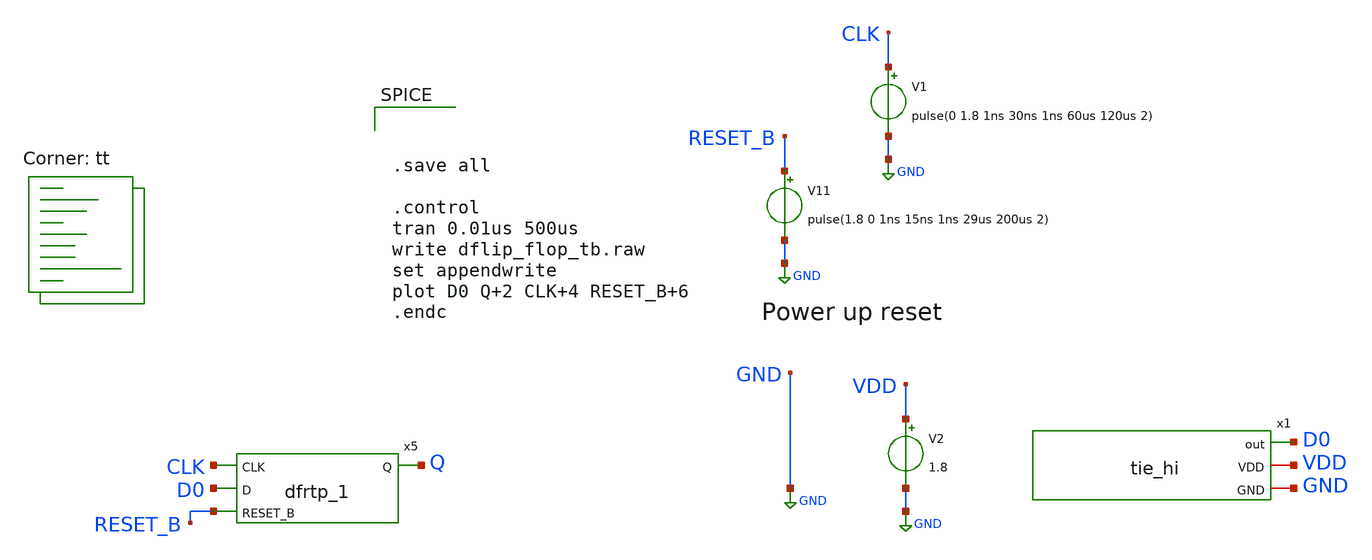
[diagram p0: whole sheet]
** sch_path: design/xschem/dflip_flop_tb.sch
**.subckt dflip_flop_tb
x5 CLK D0 RESET_B VGND VNB VPB VPWR Q sky130_fd_sc_hd__dfrtp_1
V11 RESET_B GND pulse(1.8 0 1ns 15ns 1ns 29us 200us 2)
V2 VDD GND 1.8
V1 CLK GND pulse(0 1.8 1ns 30ns 1ns 60us 120us 2)
x1 D0 VDD GND tie_hi
**** begin user architecture code



.save all

.control
tran 0.01us 500us
write dflip_flop_tb.raw
set appendwrite
plot D0 Q+2 CLK+4 RESET_B+6
.endc




* Standard cell simulation files
.include $::SKYWATER_STDCELLS/sky130_fd_sc_hd.spice

* Power domains
VSTDCELL_PWR VPWR 0 DC 1.8
VSTDCELL_PB  VPB  0 DC 1.8
VSTDCELL_NB  VNB  0 DC 0
VSTDCELL_GND VGND 0 DC 0
.global VNB VGND VPB VPWR


.lib $::SKYWATER_MODELS/sky130.lib.spice tt
**** end user architecture code
**.ends

* expanding   symbol:  tie_hi.sym # of pins=3
** sym_path: design/xschem/tie_hi.sym
** sch_path: design/xschem/tie_hi.sch
.subckt tie_hi out VDD GND
*.iopin VDD
*.iopin GND
*.opin out
XM4 out net1 VDD VDD sky130_fd_pr__pfet_01v8 L=0.15 W=1 nf=1 ad='int((nf+1)/2) * W/nf * 0.29' as='int((nf+2)/2) * W/nf * 0.29'
+ pd='2*int((nf+1)/2) * (W/nf + 0.29)' ps='2*int((nf+2)/2) * (W/nf + 0.29)' nrd='0.29 / W' nrs='0.29 / W'
+ sa=0 sb=0 sd=0 mult=1 m=1
XM2 net1 net1 GND GND sky130_fd_pr__nfet_01v8 L=0.15 W=0.65 nf=1 ad='int((nf+1)/2) * W/nf * 0.29' as='int((nf+2)/2) * W/nf * 0.29'
+ pd='2*int((nf+1)/2) * (W/nf + 0.29)' ps='2*int((nf+2)/2) * (W/nf + 0.29)' nrd='0.29 / W' nrs='0.29 / W'
+ sa=0 sb=0 sd=0 mult=1 m=1
.ends

.GLOBAL GND
.end
